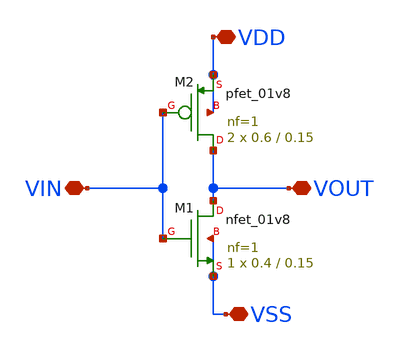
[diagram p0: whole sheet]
** sch_path: xschem/DC_DC_Converter_xschem/DC_DC_Converter/Delay_block_revised/inverter_delay.sch
**.subckt inverter_delay VDD VOUT VSS VIN
*.iopin VDD
*.iopin VOUT
*.iopin VSS
*.iopin VIN
XM1 VOUT VIN VSS VSS sky130_fd_pr__nfet_01v8 L=0.15 W=0.4 nf=1 ad='int((nf+1)/2) * W/nf * 0.29' as='int((nf+2)/2) * W/nf * 0.29'
+ pd='2*int((nf+1)/2) * (W/nf + 0.29)' ps='2*int((nf+2)/2) * (W/nf + 0.29)' nrd='0.29 / W' nrs='0.29 / W'
+ sa=0 sb=0 sd=0 mult=1 m=1
XM2 VOUT VIN VDD VDD sky130_fd_pr__pfet_01v8 L=0.15 W=0.6 nf=1 ad='int((nf+1)/2) * W/nf * 0.29' as='int((nf+2)/2) * W/nf * 0.29'
+ pd='2*int((nf+1)/2) * (W/nf + 0.29)' ps='2*int((nf+2)/2) * (W/nf + 0.29)' nrd='0.29 / W' nrs='0.29 / W'
+ sa=0 sb=0 sd=0 mult=2 m=2
**.ends
.end
